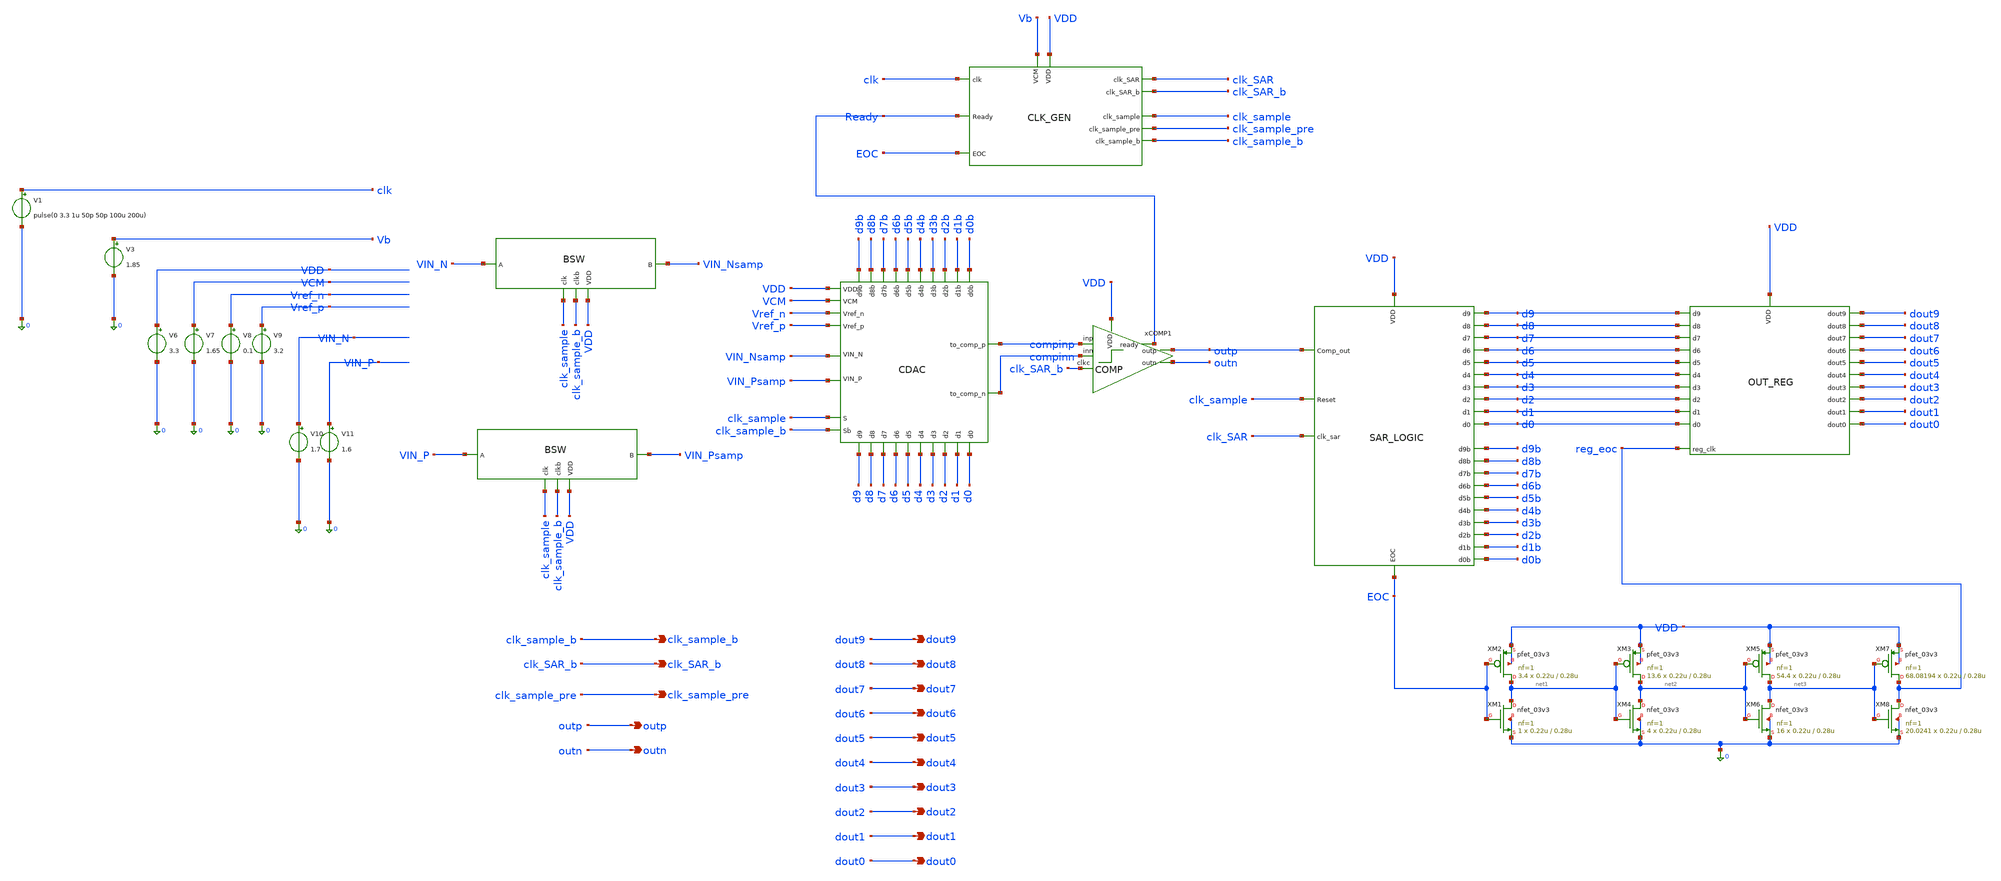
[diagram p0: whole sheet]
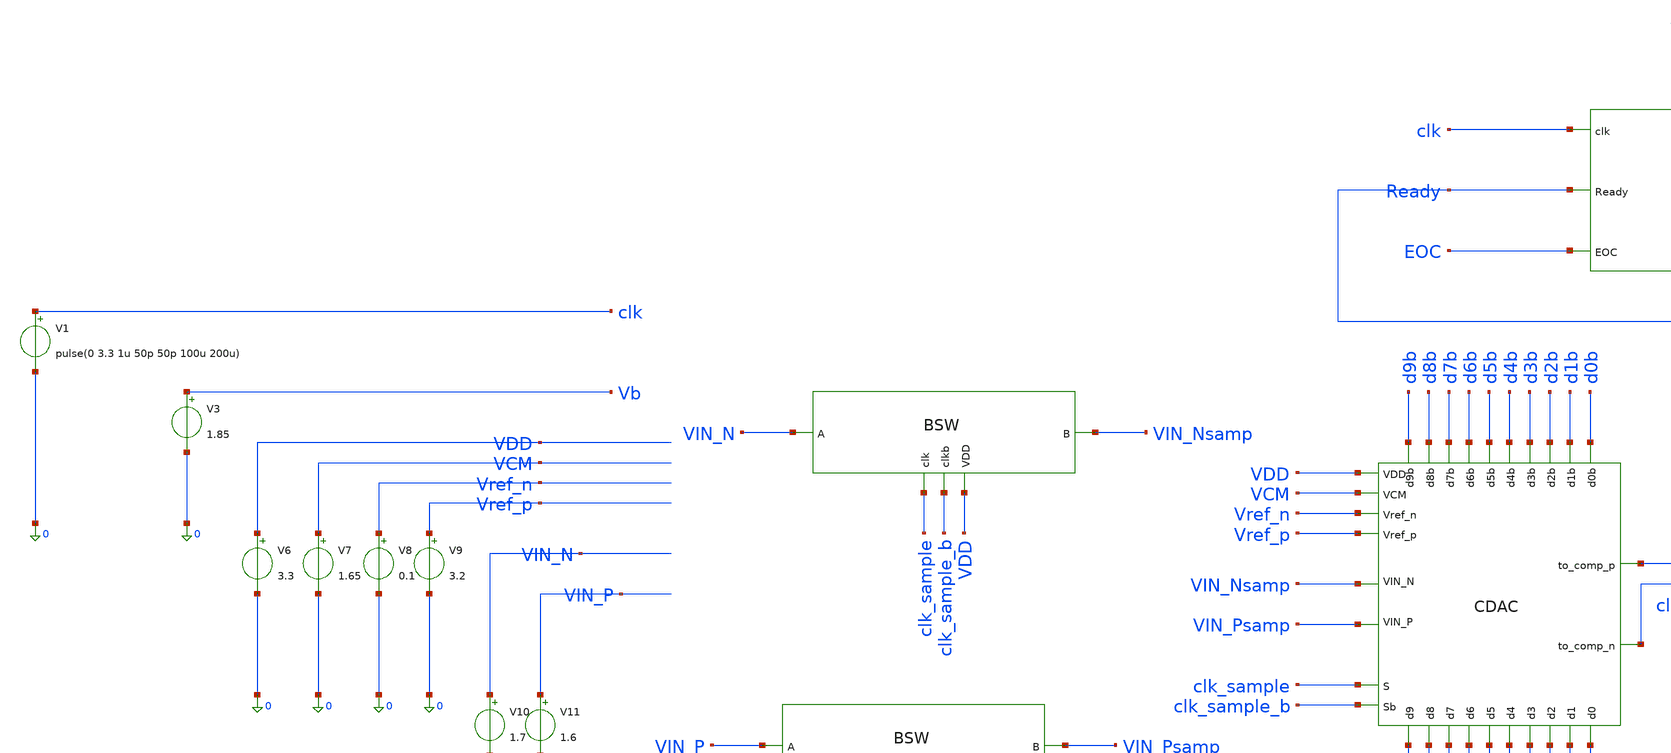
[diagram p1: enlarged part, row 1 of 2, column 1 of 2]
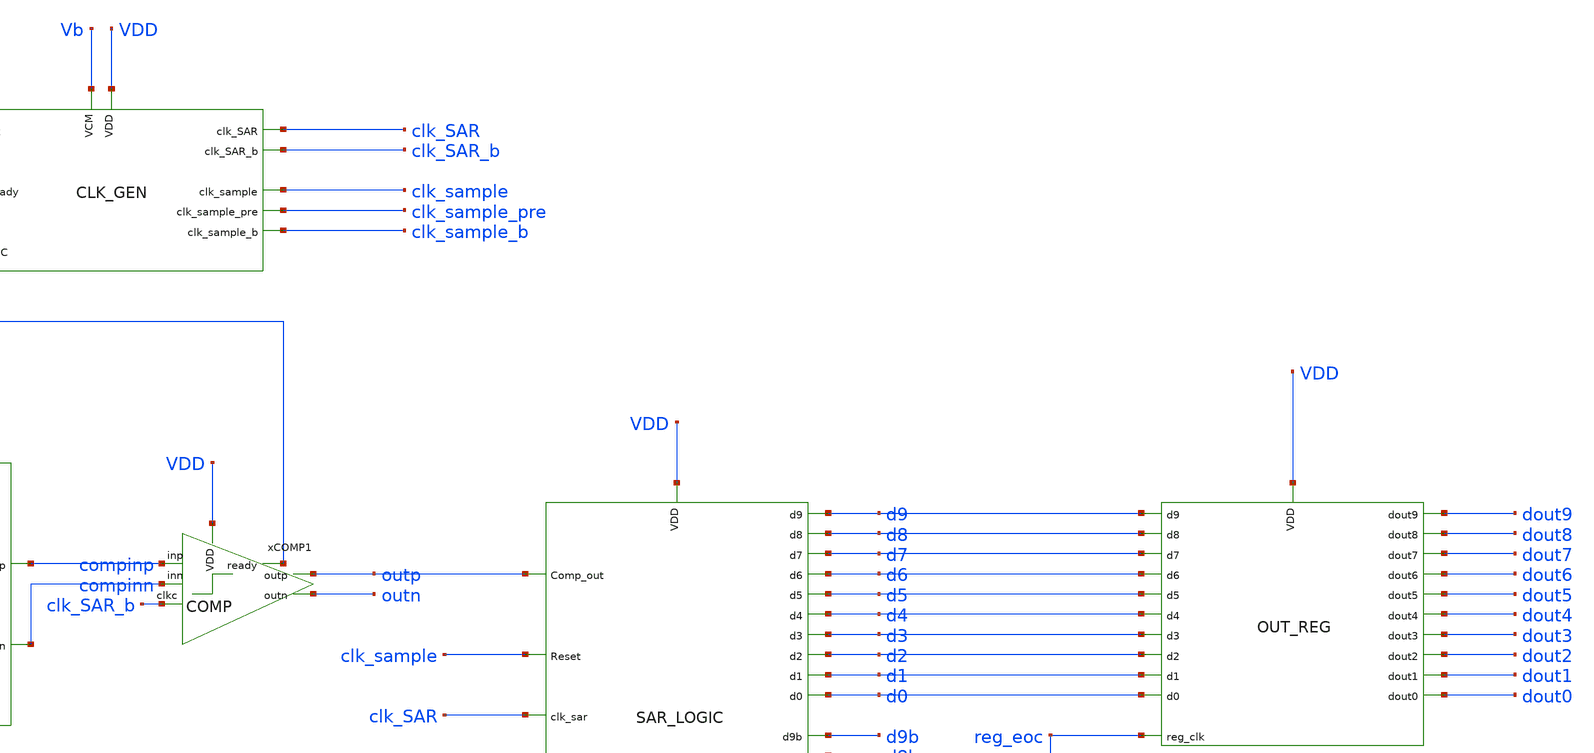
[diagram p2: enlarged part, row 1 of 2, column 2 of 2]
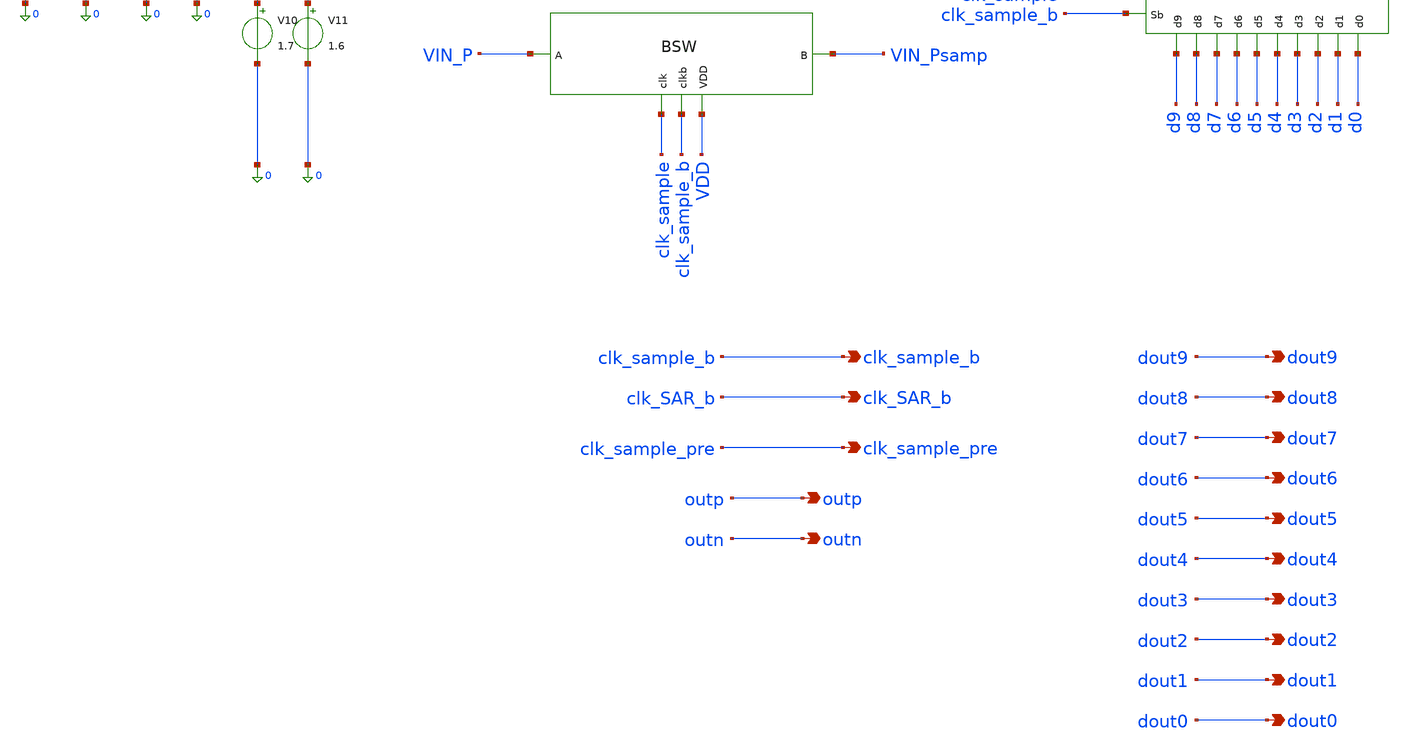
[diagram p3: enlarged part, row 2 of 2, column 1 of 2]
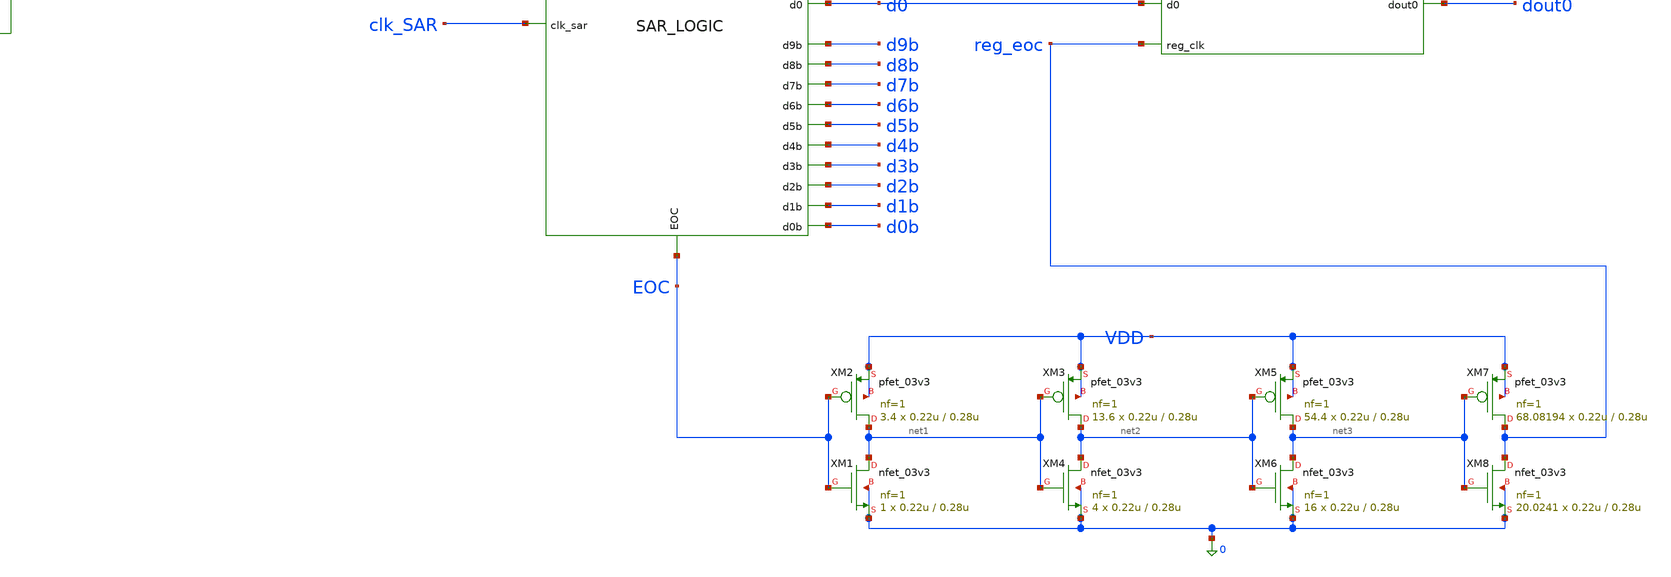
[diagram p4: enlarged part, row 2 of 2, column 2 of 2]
** sch_path: Design_Files/IC Design/Schematic/SAR_ADC_BLOCKS/SAR_ADC/SAR_ADC.sch
**.subckt SAR_ADC clk_sample_b clk_SAR_b clk_sample_pre outp outn dout9 dout8 dout7 dout6 dout5
*+ dout4 dout3 dout2 dout1 dout0
*.opin clk_sample_b
*.opin clk_SAR_b
*.opin clk_sample_pre
*.opin outp
*.opin outn
*.opin dout9
*.opin dout8
*.opin dout7
*.opin dout6
*.opin dout5
*.opin dout4
*.opin dout3
*.opin dout2
*.opin dout1
*.opin dout0
V1 clk 0 pulse(0 3.3 1u 50p 50p 100u 200u)
V3 Vb 0 1.85
V6 VDD 0 3.3
V7 VCM 0 1.65
V8 Vref_n 0 0.1
V9 Vref_p 0 3.2
V10 VIN_N 0 1.7
V11 VIN_P 0 1.6
XM2 net1 EOC VDD VDD pfet_03v3 L=0.28u W=0.22u nf=1 ad='int((nf+1)/2) * W/nf * 0.18u' as='int((nf+2)/2) * W/nf * 0.18u'
+ pd='2*int((nf+1)/2) * (W/nf + 0.18u)' ps='2*int((nf+2)/2) * (W/nf + 0.18u)' nrd='0.18u / W' nrs='0.18u / W'
+ sa=0 sb=0 sd=0 m=3.4
XM1 net1 EOC 0 0 nfet_03v3 L=0.28u W=0.22u nf=1 ad='int((nf+1)/2) * W/nf * 0.18u' as='int((nf+2)/2) * W/nf * 0.18u'
+ pd='2*int((nf+1)/2) * (W/nf + 0.18u)' ps='2*int((nf+2)/2) * (W/nf + 0.18u)' nrd='0.18u / W' nrs='0.18u / W'
+ sa=0 sb=0 sd=0 m=1
XM3 net2 net1 VDD VDD pfet_03v3 L=0.28u W=0.22u nf=1 ad='int((nf+1)/2) * W/nf * 0.18u' as='int((nf+2)/2) * W/nf * 0.18u'
+ pd='2*int((nf+1)/2) * (W/nf + 0.18u)' ps='2*int((nf+2)/2) * (W/nf + 0.18u)' nrd='0.18u / W' nrs='0.18u / W'
+ sa=0 sb=0 sd=0 m=13.6
XM4 net2 net1 0 0 nfet_03v3 L=0.28u W=0.22u nf=1 ad='int((nf+1)/2) * W/nf * 0.18u' as='int((nf+2)/2) * W/nf * 0.18u'
+ pd='2*int((nf+1)/2) * (W/nf + 0.18u)' ps='2*int((nf+2)/2) * (W/nf + 0.18u)' nrd='0.18u / W' nrs='0.18u / W'
+ sa=0 sb=0 sd=0 m=4
XM5 net3 net2 VDD VDD pfet_03v3 L=0.28u W=0.22u nf=1 ad='int((nf+1)/2) * W/nf * 0.18u' as='int((nf+2)/2) * W/nf * 0.18u'
+ pd='2*int((nf+1)/2) * (W/nf + 0.18u)' ps='2*int((nf+2)/2) * (W/nf + 0.18u)' nrd='0.18u / W' nrs='0.18u / W'
+ sa=0 sb=0 sd=0 m=54.4
XM6 net3 net2 0 0 nfet_03v3 L=0.28u W=0.22u nf=1 ad='int((nf+1)/2) * W/nf * 0.18u' as='int((nf+2)/2) * W/nf * 0.18u'
+ pd='2*int((nf+1)/2) * (W/nf + 0.18u)' ps='2*int((nf+2)/2) * (W/nf + 0.18u)' nrd='0.18u / W' nrs='0.18u / W'
+ sa=0 sb=0 sd=0 m=16
XM7 reg_eoc net3 VDD VDD pfet_03v3 L=0.28u W=0.22u nf=1 ad='int((nf+1)/2) * W/nf * 0.18u' as='int((nf+2)/2) * W/nf * 0.18u'
+ pd='2*int((nf+1)/2) * (W/nf + 0.18u)' ps='2*int((nf+2)/2) * (W/nf + 0.18u)' nrd='0.18u / W' nrs='0.18u / W'
+ sa=0 sb=0 sd=0 m=68.08194
XM8 reg_eoc net3 0 0 nfet_03v3 L=0.28u W=0.22u nf=1 ad='int((nf+1)/2) * W/nf * 0.18u' as='int((nf+2)/2) * W/nf * 0.18u'
+ pd='2*int((nf+1)/2) * (W/nf + 0.18u)' ps='2*int((nf+2)/2) * (W/nf + 0.18u)' nrd='0.18u / W' nrs='0.18u / W'
+ sa=0 sb=0 sd=0 m=20.0241
xBSW1 clk_sample clk_sample_b VDD VIN_N VIN_Nsamp BSW
xBSW2 clk_sample clk_sample_b VDD VIN_P VIN_Psamp BSW
xCLKGEN1 clk VDD Vb EOC Ready clk_sample_b clk_sample clk_SAR clk_SAR_b clk_sample_pre CLK_GEN
xCOMP1 VDD Ready compinp outp outn compinn clk_SAR_b COMP
xSARLOGIC1 outp clk_sample clk_SAR VDD EOC d9 d8 d7 d6 d5 d4 d3 d2 d1 d0 d9b d8b d7b d6b d5b d4b d3b
+ d2b d1b d0b SAR_LOGIC
xOUTREG1 d9 d8 d7 d6 d5 d4 d3 d2 d1 d0 VDD reg_eoc dout9 dout8 dout7 dout6 dout5 dout4 dout3 dout2
+ dout1 dout0 OUT_REG
xCDAC1 d9b d9 d8b d8 d7b d7 d6 d6b d5b d5 d4 d4b d3b d3 d2b d2 d1 d1b d0b d0 compinp VDD compinn VCM
+ clk_sample clk_sample_b VIN_Psamp VIN_Nsamp Vref_p Vref_n CDAC
**** begin user architecture code


.param PAR_VDD=3.3
.param m_nand=0.8
.param wp_inv=46.24
.param wn_inv=4
.param wp_inv2=115.6
.param wn_inv2=10

.control

save all

tran 100p 110u

setplot tran1

plot v(clk)+17.5 v(clk_sample)+14 v(clk_sample_pre)+10.5 v(clk_sample_b)+7 v(clk_sar)+3.5
+ v(clk_sar_b)
plot v(d9)+31.5 v(d8)+28 v(d7)+24.5 v(d6)+21 v(d5)+17.5 v(d4)+14 v(d3)+10.5 v(d2)+7 v(d1)+3.5 v(d0)
plot v(reg_eoc)+20.5 v(EOC)+17 v(compinp)+13.5 v(compinn)+13.5 v(clk_sar_b)+10.5 v(ready)+7
+ v(outp)+3.5 v(outn)
plot v(compinp)+10.5 v(compinn)+10.5 v(compinp)-v(compinn)+7 v(outp)+3.5 v(outn)
plot v(dout0) v(dout1)+3.5 v(dout2)+7 v(dout3)+10.5 v(dout4)+14 v(dout5)+17.5 v(dout6)+21
+ v(dout7)+24.5 v(dout8)+28 v(dout9)+31.5 v(reg_eoc)+35
plot VIN_Nsamp VIN_Psamp
**plot v(xSARLOGIC1.seq_start)+10.5 v(xSARLOGIC1.seq9)+7 v(xSARLOGIC1.seq8)+3.5 v(xSARLOGIC1.seq7)
**plot v(xSARLOGIC1.seq6)+10.5 v(xSARLOGIC1.seq5)+7 v(xSARLOGIC1.seq4)+3.5 v(xSARLOGIC1.seq3)
**plot v(xSARLOGIC1.seq_start)+10.5 v(xSARLOGIC1.seq9)+10.5 v(xSARLOGIC1.seq8)+10.5 v(d9)+7
*+ v(d8)+3.5 v(d7)
**plot v(xCDAC1.D9_P)+10.5 v(xCDAC1.D8_P)+7 v(xCDAC1.D7_P)+3.5 v(xCDAC1.D6_P)
**plot v(xCDAC1.D9_N)+10.5 v(xCDAC1.D8_N)+7 v(xCDAC1.D7_N)+3.5 v(xCDAC1.D6_N)
**plot v(d9)+10.5 v(d9b)+10.5 v(d8)+7 v(d8b)+7 v(d7)+3.5 v(d7b)+3.5 v(d6) v(d6b)
**plot v(d9) v(d9b) v(clk_sample_pre)+3.5 v(clk_sample_b)+3.5 v(xCDAC1.D9_P)+7 v(Vref_n)+10.5
*+ v(VIN_N)+10.5
**plot v(clk)+7 v(xCLKGEN1.clkpre)+3.5 v(xCLKGEN1.clk_delay)
**plot v(xCLKGEN1.Reset)+14 v(xCLKGEN1.Set_pre)+10.5 v(Ready)+7 v(xCLKGEN1.q)+3.5
*+ v(xCLKGEN1.clk_sar_pre)
plot v(xSARLOGIC1.xTSPCFF2.Q_bar_pre)+24.5 v(xSARLOGIC1.xTSPCFF2.Q_1st)+21
+ v(xSARLOGIC1.xTSPCFF2.Q_pre)+17.5 v(xSARLOGIC1.seq8)+14 v(xSARLOGIC1.seq_start)+10.5 v(xSARLOGIC1.seq9)+7 v(clk_sample)+3.5
+ v(clk_sar)
.endc



.include $::180MCU_MODELS/design.ngspice
.lib $::180MCU_MODELS/sm141064.ngspice ss
.lib $::180MCU_MODELS/smbb000149.ngspice ss

**** end user architecture code
**.ends
.end
